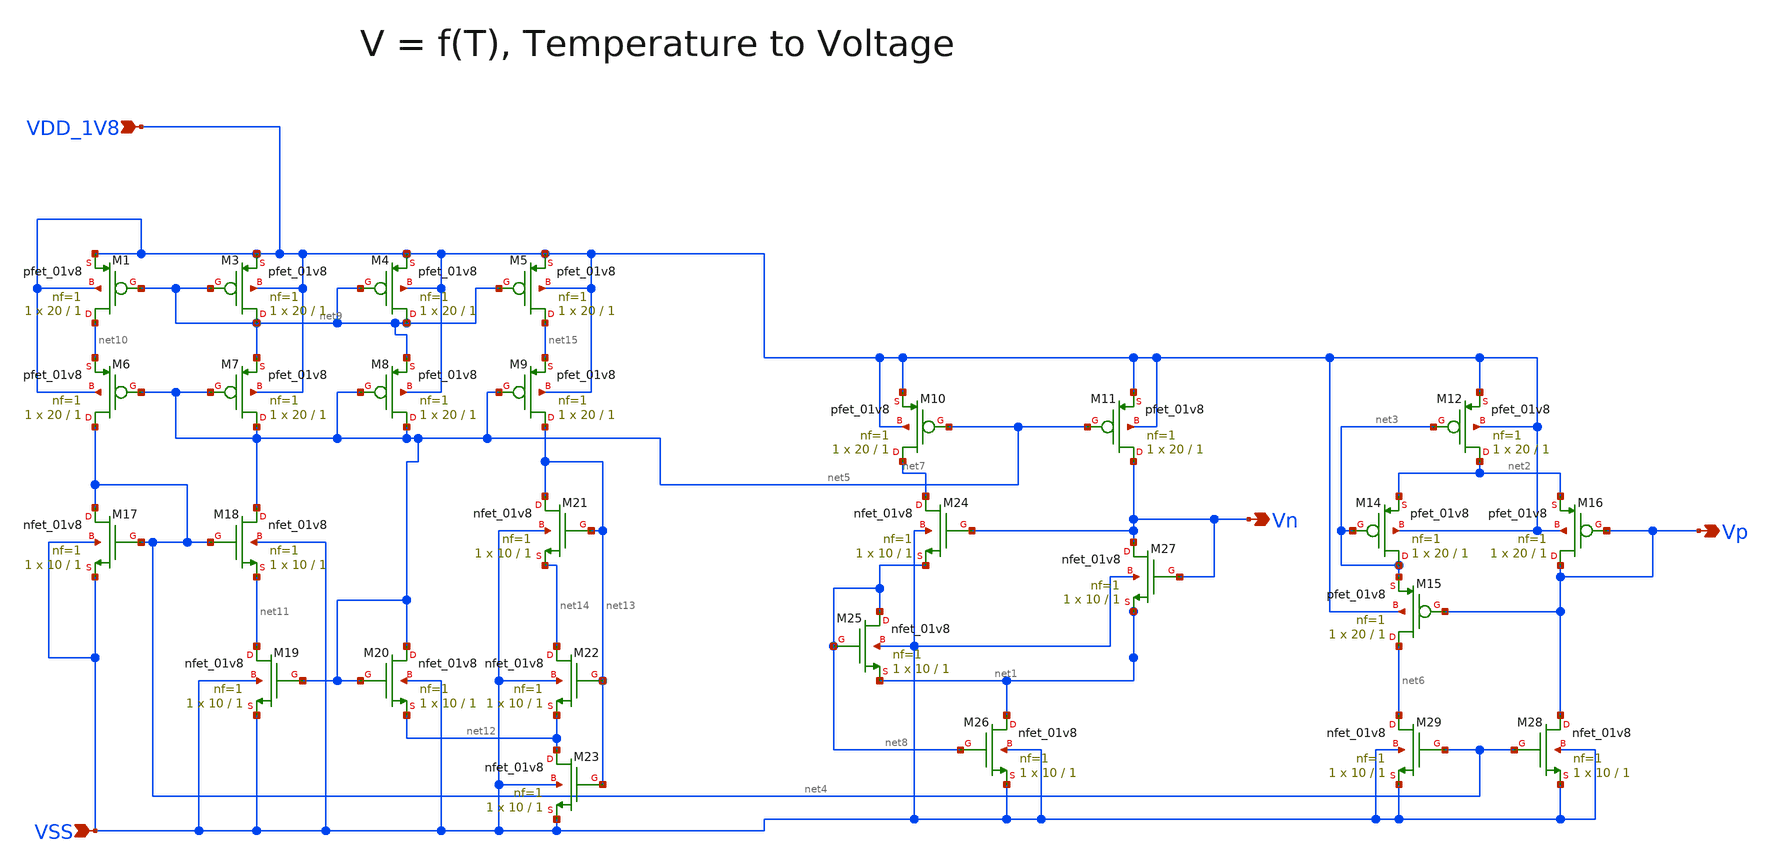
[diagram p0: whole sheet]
** sch_path: design/CNR_GR06_SKY130NM/CNR_GR06_test.sch
**.subckt CNR_GR06_test VDD_1V8 VSS Vn Vp
*.ipin VDD_1V8
*.ipin VSS
*.opin Vn
*.opin Vp
XM1 net10 net9 VDD_1V8 VDD_1V8 sky130_fd_pr__pfet_01v8 L=1 W=20 nf=1 ad='int((nf+1)/2) * W/nf * 0.29'
+ as='int((nf+2)/2) * W/nf * 0.29' pd='2*int((nf+1)/2) * (W/nf + 0.29)' ps='2*int((nf+2)/2) * (W/nf + 0.29)'
+ nrd='0.29 / W' nrs='0.29 / W' sa=0 sb=0 sd=0 mult=1 m=1
XM3 net9 net9 VDD_1V8 VDD_1V8 sky130_fd_pr__pfet_01v8 L=1 W=20 nf=1 ad='int((nf+1)/2) * W/nf * 0.29'
+ as='int((nf+2)/2) * W/nf * 0.29' pd='2*int((nf+1)/2) * (W/nf + 0.29)' ps='2*int((nf+2)/2) * (W/nf + 0.29)'
+ nrd='0.29 / W' nrs='0.29 / W' sa=0 sb=0 sd=0 mult=1 m=1
XM4 net9 net9 VDD_1V8 VDD_1V8 sky130_fd_pr__pfet_01v8 L=1 W=20 nf=1 ad='int((nf+1)/2) * W/nf * 0.29'
+ as='int((nf+2)/2) * W/nf * 0.29' pd='2*int((nf+1)/2) * (W/nf + 0.29)' ps='2*int((nf+2)/2) * (W/nf + 0.29)'
+ nrd='0.29 / W' nrs='0.29 / W' sa=0 sb=0 sd=0 mult=1 m=1
XM5 net15 net9 VDD_1V8 VDD_1V8 sky130_fd_pr__pfet_01v8 L=1 W=20 nf=1 ad='int((nf+1)/2) * W/nf * 0.29'
+ as='int((nf+2)/2) * W/nf * 0.29' pd='2*int((nf+1)/2) * (W/nf + 0.29)' ps='2*int((nf+2)/2) * (W/nf + 0.29)'
+ nrd='0.29 / W' nrs='0.29 / W' sa=0 sb=0 sd=0 mult=1 m=1
XM6 net4 net5 net10 VDD_1V8 sky130_fd_pr__pfet_01v8 L=1 W=20 nf=1 ad='int((nf+1)/2) * W/nf * 0.29' as='int((nf+2)/2) * W/nf * 0.29'
+ pd='2*int((nf+1)/2) * (W/nf + 0.29)' ps='2*int((nf+2)/2) * (W/nf + 0.29)' nrd='0.29 / W' nrs='0.29 / W'
+ sa=0 sb=0 sd=0 mult=1 m=1
XM7 net5 net5 net9 VDD_1V8 sky130_fd_pr__pfet_01v8 L=1 W=20 nf=1 ad='int((nf+1)/2) * W/nf * 0.29' as='int((nf+2)/2) * W/nf * 0.29'
+ pd='2*int((nf+1)/2) * (W/nf + 0.29)' ps='2*int((nf+2)/2) * (W/nf + 0.29)' nrd='0.29 / W' nrs='0.29 / W'
+ sa=0 sb=0 sd=0 mult=1 m=1
XM8 net5 net5 net9 VDD_1V8 sky130_fd_pr__pfet_01v8 L=1 W=20 nf=1 ad='int((nf+1)/2) * W/nf * 0.29' as='int((nf+2)/2) * W/nf * 0.29'
+ pd='2*int((nf+1)/2) * (W/nf + 0.29)' ps='2*int((nf+2)/2) * (W/nf + 0.29)' nrd='0.29 / W' nrs='0.29 / W'
+ sa=0 sb=0 sd=0 mult=1 m=1
XM9 net13 net5 net15 VDD_1V8 sky130_fd_pr__pfet_01v8 L=1 W=20 nf=1 ad='int((nf+1)/2) * W/nf * 0.29' as='int((nf+2)/2) * W/nf * 0.29'
+ pd='2*int((nf+1)/2) * (W/nf + 0.29)' ps='2*int((nf+2)/2) * (W/nf + 0.29)' nrd='0.29 / W' nrs='0.29 / W'
+ sa=0 sb=0 sd=0 mult=1 m=1
XM10 net7 net5 VDD_1V8 VDD_1V8 sky130_fd_pr__pfet_01v8 L=1 W=20 nf=1 ad='int((nf+1)/2) * W/nf * 0.29'
+ as='int((nf+2)/2) * W/nf * 0.29' pd='2*int((nf+1)/2) * (W/nf + 0.29)' ps='2*int((nf+2)/2) * (W/nf + 0.29)'
+ nrd='0.29 / W' nrs='0.29 / W' sa=0 sb=0 sd=0 mult=1 m=1
XM11 Vn net5 VDD_1V8 VDD_1V8 sky130_fd_pr__pfet_01v8 L=1 W=20 nf=1 ad='int((nf+1)/2) * W/nf * 0.29' as='int((nf+2)/2) * W/nf * 0.29'
+ pd='2*int((nf+1)/2) * (W/nf + 0.29)' ps='2*int((nf+2)/2) * (W/nf + 0.29)' nrd='0.29 / W' nrs='0.29 / W'
+ sa=0 sb=0 sd=0 mult=1 m=1
XM12 net2 net3 VDD_1V8 VDD_1V8 sky130_fd_pr__pfet_01v8 L=1 W=20 nf=1 ad='int((nf+1)/2) * W/nf * 0.29'
+ as='int((nf+2)/2) * W/nf * 0.29' pd='2*int((nf+1)/2) * (W/nf + 0.29)' ps='2*int((nf+2)/2) * (W/nf + 0.29)'
+ nrd='0.29 / W' nrs='0.29 / W' sa=0 sb=0 sd=0 mult=1 m=1
XM14 net3 net3 net2 VDD_1V8 sky130_fd_pr__pfet_01v8 L=1 W=20 nf=1 ad='int((nf+1)/2) * W/nf * 0.29' as='int((nf+2)/2) * W/nf * 0.29'
+ pd='2*int((nf+1)/2) * (W/nf + 0.29)' ps='2*int((nf+2)/2) * (W/nf + 0.29)' nrd='0.29 / W' nrs='0.29 / W'
+ sa=0 sb=0 sd=0 mult=1 m=1
XM15 net6 Vp net3 VDD_1V8 sky130_fd_pr__pfet_01v8 L=1 W=20 nf=1 ad='int((nf+1)/2) * W/nf * 0.29' as='int((nf+2)/2) * W/nf * 0.29'
+ pd='2*int((nf+1)/2) * (W/nf + 0.29)' ps='2*int((nf+2)/2) * (W/nf + 0.29)' nrd='0.29 / W' nrs='0.29 / W'
+ sa=0 sb=0 sd=0 mult=1 m=1
XM16 Vp Vp net2 VDD_1V8 sky130_fd_pr__pfet_01v8 L=1 W=20 nf=1 ad='int((nf+1)/2) * W/nf * 0.29' as='int((nf+2)/2) * W/nf * 0.29'
+ pd='2*int((nf+1)/2) * (W/nf + 0.29)' ps='2*int((nf+2)/2) * (W/nf + 0.29)' nrd='0.29 / W' nrs='0.29 / W'
+ sa=0 sb=0 sd=0 mult=1 m=1
XM17 net4 net4 VSS VSS sky130_fd_pr__nfet_01v8 L=1 W=10 nf=1 ad='int((nf+1)/2) * W/nf * 0.29' as='int((nf+2)/2) * W/nf * 0.29'
+ pd='2*int((nf+1)/2) * (W/nf + 0.29)' ps='2*int((nf+2)/2) * (W/nf + 0.29)' nrd='0.29 / W' nrs='0.29 / W'
+ sa=0 sb=0 sd=0 mult=1 m=1
XM18 net5 net4 net11 VSS sky130_fd_pr__nfet_01v8 L=1 W=10 nf=1 ad='int((nf+1)/2) * W/nf * 0.29' as='int((nf+2)/2) * W/nf * 0.29'
+ pd='2*int((nf+1)/2) * (W/nf + 0.29)' ps='2*int((nf+2)/2) * (W/nf + 0.29)' nrd='0.29 / W' nrs='0.29 / W'
+ sa=0 sb=0 sd=0 mult=1 m=1
XM19 net11 net5 VSS VSS sky130_fd_pr__nfet_01v8 L=1 W=10 nf=1 ad='int((nf+1)/2) * W/nf * 0.29' as='int((nf+2)/2) * W/nf * 0.29'
+ pd='2*int((nf+1)/2) * (W/nf + 0.29)' ps='2*int((nf+2)/2) * (W/nf + 0.29)' nrd='0.29 / W' nrs='0.29 / W'
+ sa=0 sb=0 sd=0 mult=1 m=1
XM20 net5 net5 net12 VSS sky130_fd_pr__nfet_01v8 L=1 W=10 nf=1 ad='int((nf+1)/2) * W/nf * 0.29' as='int((nf+2)/2) * W/nf * 0.29'
+ pd='2*int((nf+1)/2) * (W/nf + 0.29)' ps='2*int((nf+2)/2) * (W/nf + 0.29)' nrd='0.29 / W' nrs='0.29 / W'
+ sa=0 sb=0 sd=0 mult=1 m=1
XM21 net13 net13 net14 VSS sky130_fd_pr__nfet_01v8 L=1 W=10 nf=1 ad='int((nf+1)/2) * W/nf * 0.29' as='int((nf+2)/2) * W/nf * 0.29'
+ pd='2*int((nf+1)/2) * (W/nf + 0.29)' ps='2*int((nf+2)/2) * (W/nf + 0.29)' nrd='0.29 / W' nrs='0.29 / W'
+ sa=0 sb=0 sd=0 mult=1 m=1
XM22 net14 net13 net12 VSS sky130_fd_pr__nfet_01v8 L=1 W=10 nf=1 ad='int((nf+1)/2) * W/nf * 0.29' as='int((nf+2)/2) * W/nf * 0.29'
+ pd='2*int((nf+1)/2) * (W/nf + 0.29)' ps='2*int((nf+2)/2) * (W/nf + 0.29)' nrd='0.29 / W' nrs='0.29 / W'
+ sa=0 sb=0 sd=0 mult=1 m=1
XM23 net12 net13 VSS VSS sky130_fd_pr__nfet_01v8 L=1 W=10 nf=1 ad='int((nf+1)/2) * W/nf * 0.29' as='int((nf+2)/2) * W/nf * 0.29'
+ pd='2*int((nf+1)/2) * (W/nf + 0.29)' ps='2*int((nf+2)/2) * (W/nf + 0.29)' nrd='0.29 / W' nrs='0.29 / W'
+ sa=0 sb=0 sd=0 mult=1 m=1
XM24 net7 Vn net8 VSS sky130_fd_pr__nfet_01v8 L=1 W=10 nf=1 ad='int((nf+1)/2) * W/nf * 0.29' as='int((nf+2)/2) * W/nf * 0.29'
+ pd='2*int((nf+1)/2) * (W/nf + 0.29)' ps='2*int((nf+2)/2) * (W/nf + 0.29)' nrd='0.29 / W' nrs='0.29 / W'
+ sa=0 sb=0 sd=0 mult=1 m=1
XM25 net8 net8 net1 VSS sky130_fd_pr__nfet_01v8 L=1 W=10 nf=1 ad='int((nf+1)/2) * W/nf * 0.29' as='int((nf+2)/2) * W/nf * 0.29'
+ pd='2*int((nf+1)/2) * (W/nf + 0.29)' ps='2*int((nf+2)/2) * (W/nf + 0.29)' nrd='0.29 / W' nrs='0.29 / W'
+ sa=0 sb=0 sd=0 mult=1 m=1
XM26 net1 net8 VSS VSS sky130_fd_pr__nfet_01v8 L=1 W=10 nf=1 ad='int((nf+1)/2) * W/nf * 0.29' as='int((nf+2)/2) * W/nf * 0.29'
+ pd='2*int((nf+1)/2) * (W/nf + 0.29)' ps='2*int((nf+2)/2) * (W/nf + 0.29)' nrd='0.29 / W' nrs='0.29 / W'
+ sa=0 sb=0 sd=0 mult=1 m=1
XM27 Vn Vn net1 VSS sky130_fd_pr__nfet_01v8 L=1 W=10 nf=1 ad='int((nf+1)/2) * W/nf * 0.29' as='int((nf+2)/2) * W/nf * 0.29'
+ pd='2*int((nf+1)/2) * (W/nf + 0.29)' ps='2*int((nf+2)/2) * (W/nf + 0.29)' nrd='0.29 / W' nrs='0.29 / W'
+ sa=0 sb=0 sd=0 mult=1 m=1
XM28 Vp net4 VSS VSS sky130_fd_pr__nfet_01v8 L=1 W=10 nf=1 ad='int((nf+1)/2) * W/nf * 0.29' as='int((nf+2)/2) * W/nf * 0.29'
+ pd='2*int((nf+1)/2) * (W/nf + 0.29)' ps='2*int((nf+2)/2) * (W/nf + 0.29)' nrd='0.29 / W' nrs='0.29 / W'
+ sa=0 sb=0 sd=0 mult=1 m=1
XM29 net6 net4 VSS VSS sky130_fd_pr__nfet_01v8 L=1 W=10 nf=1 ad='int((nf+1)/2) * W/nf * 0.29' as='int((nf+2)/2) * W/nf * 0.29'
+ pd='2*int((nf+1)/2) * (W/nf + 0.29)' ps='2*int((nf+2)/2) * (W/nf + 0.29)' nrd='0.29 / W' nrs='0.29 / W'
+ sa=0 sb=0 sd=0 mult=1 m=1
**.ends
.end
